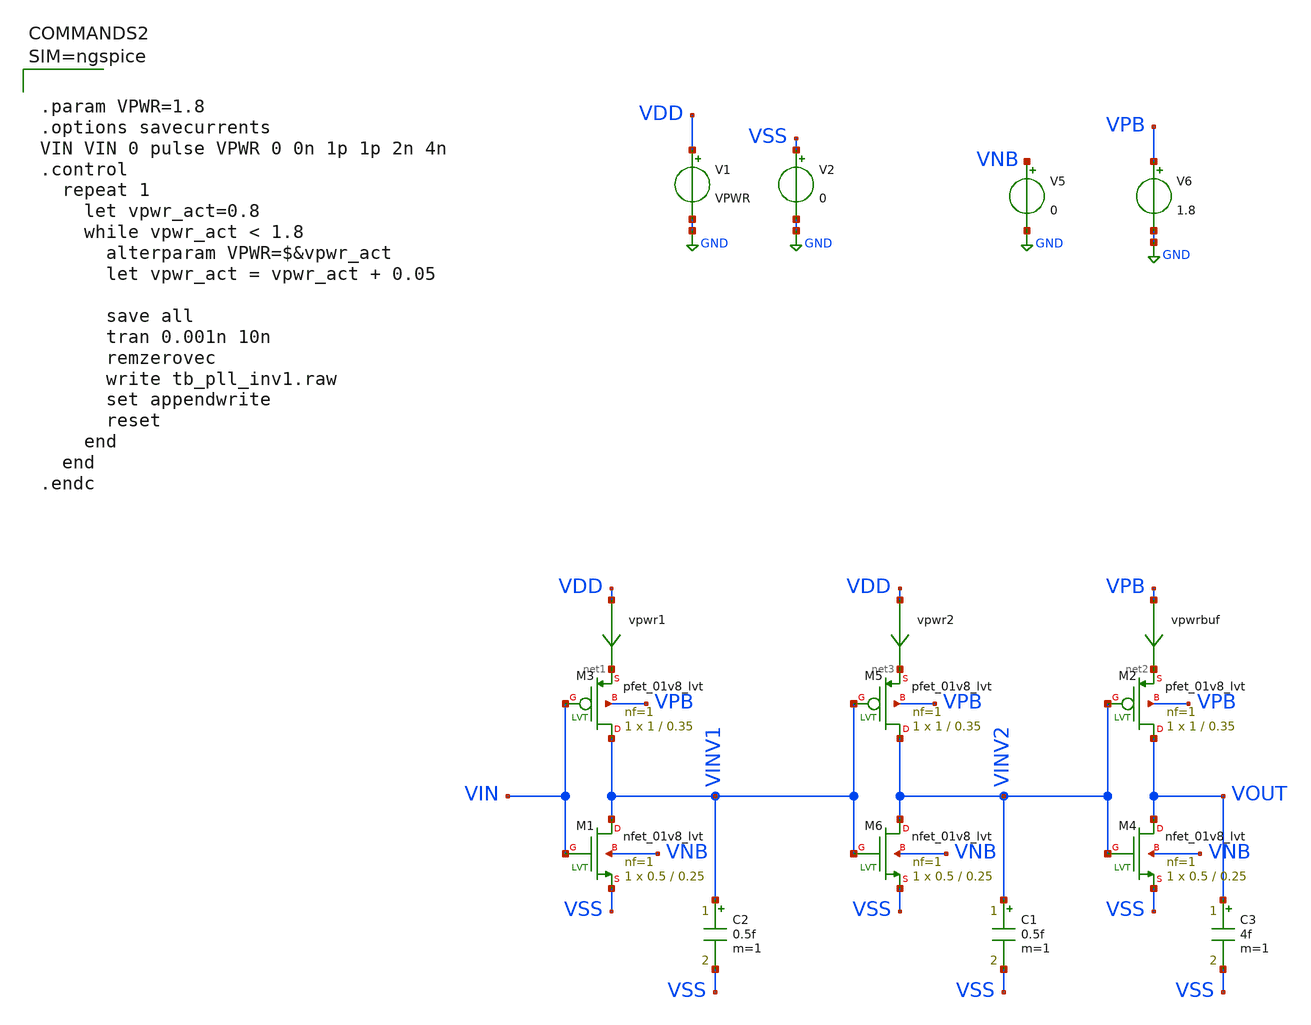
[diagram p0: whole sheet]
** sch_path: xschem/tb_pll_inv1.sch
**.subckt tb_pll_inv1
V5 VNB GND 0
V6 VPB GND 1.8
V2 VSS GND 0
XM3 VINV1 VIN net1 VPB sky130_fd_pr__pfet_01v8_lvt L=0.35 W=1 nf=1 ad='int((nf+1)/2) * W/nf * 0.29' as='int((nf+2)/2) * W/nf * 0.29'
+ pd='2*int((nf+1)/2) * (W/nf + 0.29)' ps='2*int((nf+2)/2) * (W/nf + 0.29)' nrd='0.29 / W' nrs='0.29 / W'
+ sa=0 sb=0 sd=0 mult=1 m=1
vpwr1 VDD net1 0
.save i(vpwr1)
V1 VDD GND VPWR
XM1 VINV1 VIN VSS VNB sky130_fd_pr__nfet_01v8_lvt L=0.25 W=0.5 nf=1 ad='int((nf+1)/2) * W/nf * 0.29'
+ as='int((nf+2)/2) * W/nf * 0.29' pd='2*int((nf+1)/2) * (W/nf + 0.29)' ps='2*int((nf+2)/2) * (W/nf + 0.29)'
+ nrd='0.29 / W' nrs='0.29 / W' sa=0 sb=0 sd=0 mult=1 m=1
XM2 VOUT VINV2 net2 VPB sky130_fd_pr__pfet_01v8_lvt L=0.35 W=1 nf=1 ad='int((nf+1)/2) * W/nf * 0.29'
+ as='int((nf+2)/2) * W/nf * 0.29' pd='2*int((nf+1)/2) * (W/nf + 0.29)' ps='2*int((nf+2)/2) * (W/nf + 0.29)'
+ nrd='0.29 / W' nrs='0.29 / W' sa=0 sb=0 sd=0 mult=1 m=1
vpwrbuf VPB net2 0
.save i(vpwrbuf)
XM4 VOUT VINV2 VSS VNB sky130_fd_pr__nfet_01v8_lvt L=0.25 W=0.5 nf=1 ad='int((nf+1)/2) * W/nf * 0.29'
+ as='int((nf+2)/2) * W/nf * 0.29' pd='2*int((nf+1)/2) * (W/nf + 0.29)' ps='2*int((nf+2)/2) * (W/nf + 0.29)'
+ nrd='0.29 / W' nrs='0.29 / W' sa=0 sb=0 sd=0 mult=1 m=1
C2 VINV1 VSS 0.5f m=1
C3 VOUT VSS 4f m=1
XM5 VINV2 VINV1 net3 VPB sky130_fd_pr__pfet_01v8_lvt L=0.35 W=1 nf=1 ad='int((nf+1)/2) * W/nf * 0.29'
+ as='int((nf+2)/2) * W/nf * 0.29' pd='2*int((nf+1)/2) * (W/nf + 0.29)' ps='2*int((nf+2)/2) * (W/nf + 0.29)'
+ nrd='0.29 / W' nrs='0.29 / W' sa=0 sb=0 sd=0 mult=1 m=1
vpwr2 VDD net3 0
.save i(vpwr2)
XM6 VINV2 VINV1 VSS VNB sky130_fd_pr__nfet_01v8_lvt L=0.25 W=0.5 nf=1 ad='int((nf+1)/2) * W/nf * 0.29'
+ as='int((nf+2)/2) * W/nf * 0.29' pd='2*int((nf+1)/2) * (W/nf + 0.29)' ps='2*int((nf+2)/2) * (W/nf + 0.29)'
+ nrd='0.29 / W' nrs='0.29 / W' sa=0 sb=0 sd=0 mult=1 m=1
C1 VINV2 VSS 0.5f m=1
**** begin user architecture code

** opencircuitdesign pdks install
.lib $::SKYWATER_MODELS/sky130.lib.spice tt_mm
*.lib $::SKYWATER_STDCELLS/sky130_fd_sc_hd_blablabla.spice

.subckt sky130_fd_sc_hd__inv_1 A VGND VNB VPB VPWR Y
X0 VGND A Y VNB sky130_fd_pr__nfet_01v8 w=650000u l=150000u
X1 VPWR A Y VPB sky130_fd_pr__pfet_01v8_hvt w=1e+06u l=150000u
.ends





.param VPWR=1.8
.options savecurrents
VIN VIN 0 pulse VPWR 0 0n 1p 1p 2n 4n
.control
  repeat 1
    let vpwr_act=0.8
    while vpwr_act < 1.8
      alterparam VPWR=$&vpwr_act
      let vpwr_act = vpwr_act + 0.05

      save all
      tran 0.001n 10n
      remzerovec
      write tb_pll_inv1.raw
      set appendwrite
      reset
    end
  end
.endc



**** end user architecture code
**.ends
.GLOBAL GND
.end
